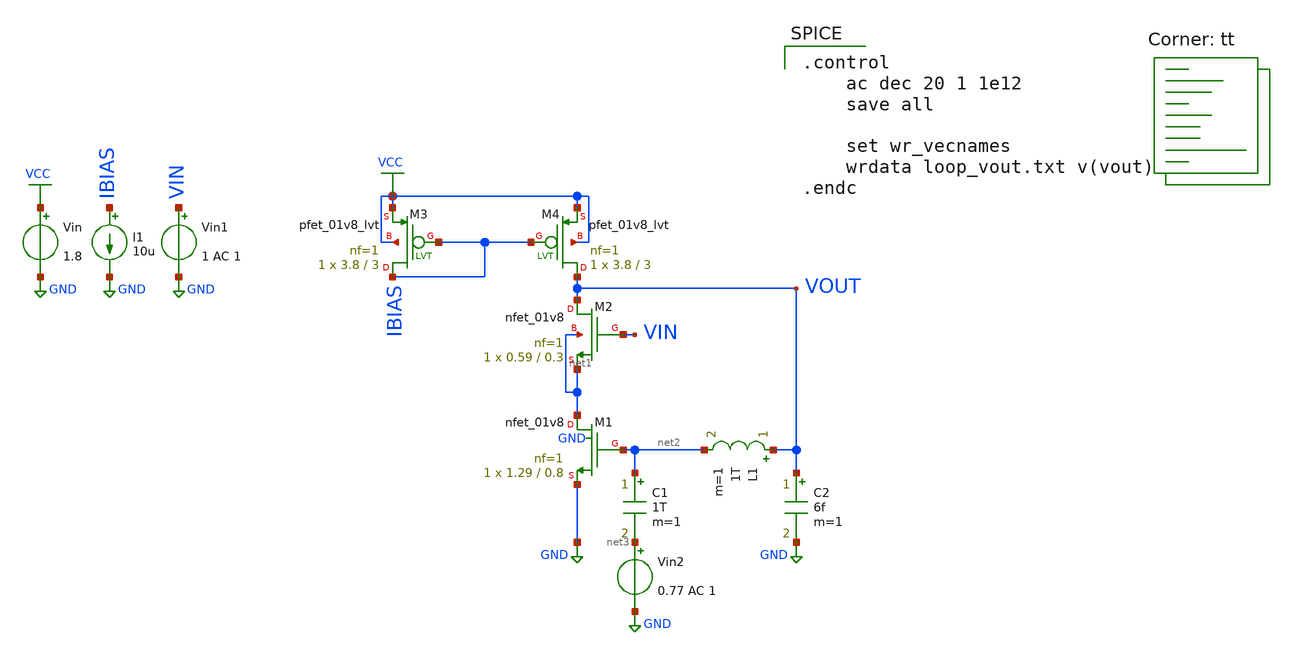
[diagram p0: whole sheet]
** sch_path: xschem/fvf_tb_loop.sch
**.subckt fvf_tb_loop
Vin VCC GND 1.8
Vin1 VIN GND 1 AC 1
I1 IBIAS GND 10u
L1 VOUT net2 1T m=1
C1 net2 net3 1T m=1
C2 VOUT GND 6f m=1
XM3 IBIAS IBIAS VCC VCC sky130_fd_pr__pfet_01v8_lvt L=3 W=3.8 nf=1 ad='int((nf+1)/2) * W/nf * 0.29' as='int((nf+2)/2) * W/nf * 0.29'
+ pd='2*int((nf+1)/2) * (W/nf + 0.29)' ps='2*int((nf+2)/2) * (W/nf + 0.29)' nrd='0.29 / W' nrs='0.29 / W'
+ sa=0 sb=0 sd=0 mult=1 m=1
XM4 VOUT IBIAS VCC VCC sky130_fd_pr__pfet_01v8_lvt L=3 W=3.8 nf=1 ad='int((nf+1)/2) * W/nf * 0.29' as='int((nf+2)/2) * W/nf * 0.29'
+ pd='2*int((nf+1)/2) * (W/nf + 0.29)' ps='2*int((nf+2)/2) * (W/nf + 0.29)' nrd='0.29 / W' nrs='0.29 / W'
+ sa=0 sb=0 sd=0 mult=1 m=1
Vin2 net3 GND 0.77 AC 1
XM1 net1 net2 GND GND sky130_fd_pr__nfet_01v8 L=0.8 W=1.29 nf=1 ad='int((nf+1)/2) * W/nf * 0.29' as='int((nf+2)/2) * W/nf * 0.29'
+ pd='2*int((nf+1)/2) * (W/nf + 0.29)' ps='2*int((nf+2)/2) * (W/nf + 0.29)' nrd='0.29 / W' nrs='0.29 / W'
+ sa=0 sb=0 sd=0 mult=1 m=1
XM2 VOUT VIN net1 net1 sky130_fd_pr__nfet_01v8 L=0.3 W=0.59 nf=1 ad='int((nf+1)/2) * W/nf * 0.29' as='int((nf+2)/2) * W/nf * 0.29'
+ pd='2*int((nf+1)/2) * (W/nf + 0.29)' ps='2*int((nf+2)/2) * (W/nf + 0.29)' nrd='0.29 / W' nrs='0.29 / W'
+ sa=0 sb=0 sd=0 mult=1 m=1
**** begin user architecture code
.lib $::SKYWATER_MODELS/sky130.lib.spice tt

.control
    ac dec 20 1 1e12
    save all

    set wr_vecnames
    wrdata loop_vout.txt v(vout)
.endc

**** end user architecture code
**.ends
.GLOBAL VCC
.GLOBAL GND
.end
